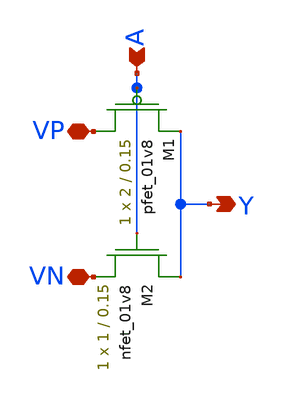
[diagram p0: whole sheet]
** sch_path: Miniproject1/inverter_LDS.sch
**.subckt inverter_LDS VP VN A Y
*.iopin VP
*.iopin VN
*.ipin A
*.opin Y
XM1 VP A Y VDD sky130_fd_pr__pfet_01v8 L=0.15 W=2 nf=1 ad='int((nf+1)/2) * W/nf * 0.29' as='int((nf+2)/2) * W/nf * 0.29'
+ pd='2*int((nf+1)/2) * (W/nf + 0.29)' ps='2*int((nf+2)/2) * (W/nf + 0.29)' nrd='0.29 / W' nrs='0.29 / W'
+ sa=0 sb=0 sd=0 mult=1 m=1
XM2 Y A VN GND sky130_fd_pr__nfet_01v8 L=0.15 W=1 nf=1 ad='int((nf+1)/2) * W/nf * 0.29' as='int((nf+2)/2) * W/nf * 0.29'
+ pd='2*int((nf+1)/2) * (W/nf + 0.29)' ps='2*int((nf+2)/2) * (W/nf + 0.29)' nrd='0.29 / W' nrs='0.29 / W'
+ sa=0 sb=0 sd=0 mult=1 m=1
**.ends
.end
